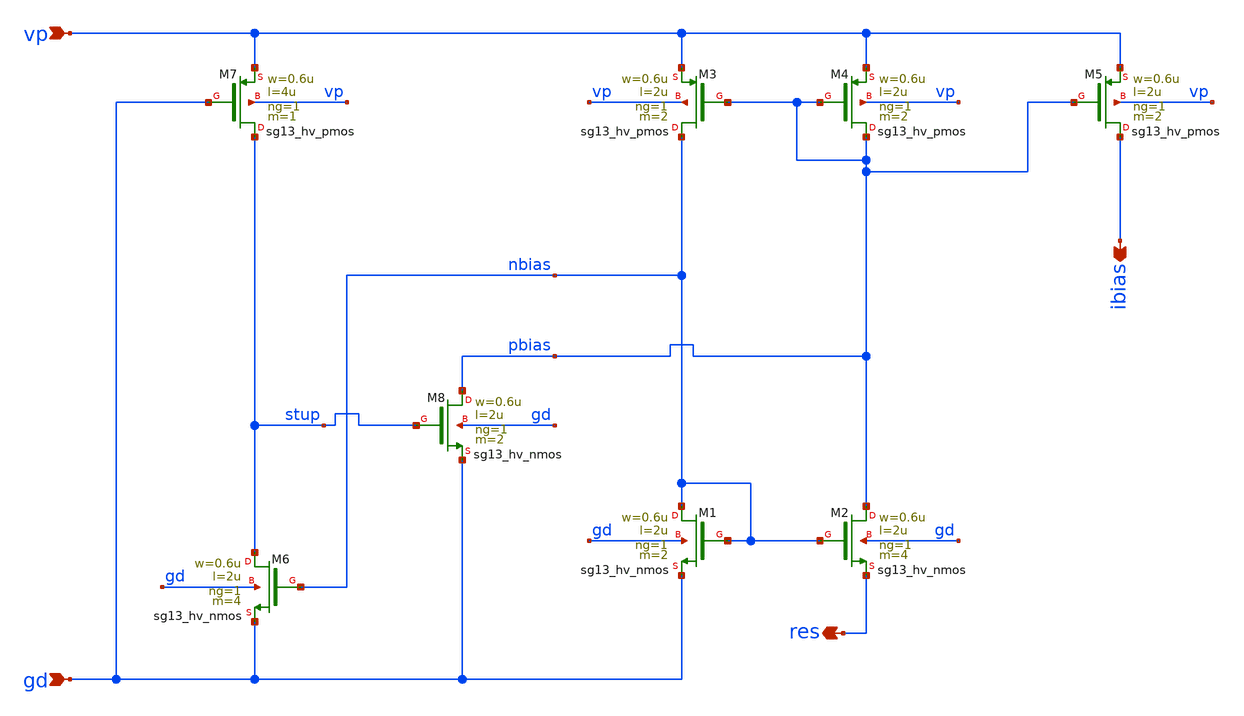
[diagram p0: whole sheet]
** sch_path: circuit/const_gm_bias_core.sch
**.subckt const_gm_bias_core vp gd ibias res
*.ipin vp
*.ipin gd
*.opin ibias
*.opin res
XM1 nbias nbias gd gd sg13_hv_nmos w=0.6u l=2u ng=1 m=2 mm_ok=1
XM2 pbias nbias res gd sg13_hv_nmos w=0.6u l=2u ng=1 m=4 mm_ok=1
XM4 pbias pbias vp vp sg13_hv_pmos w=0.6u l=2u ng=1 m=2 mm_ok=1
XM3 nbias pbias vp vp sg13_hv_pmos w=0.6u l=2u ng=1 m=2 mm_ok=1
XM5 ibias pbias vp vp sg13_hv_pmos w=0.6u l=2u ng=1 m=2 mm_ok=1
XM7 stup gd vp vp sg13_hv_pmos w=0.6u l=4u ng=1 m=1 mm_ok=1
XM6 stup nbias gd gd sg13_hv_nmos w=0.6u l=2u ng=1 m=4 mm_ok=1
XM8 pbias stup gd gd sg13_hv_nmos w=0.6u l=2u ng=1 m=2 mm_ok=1
**.ends
.end
